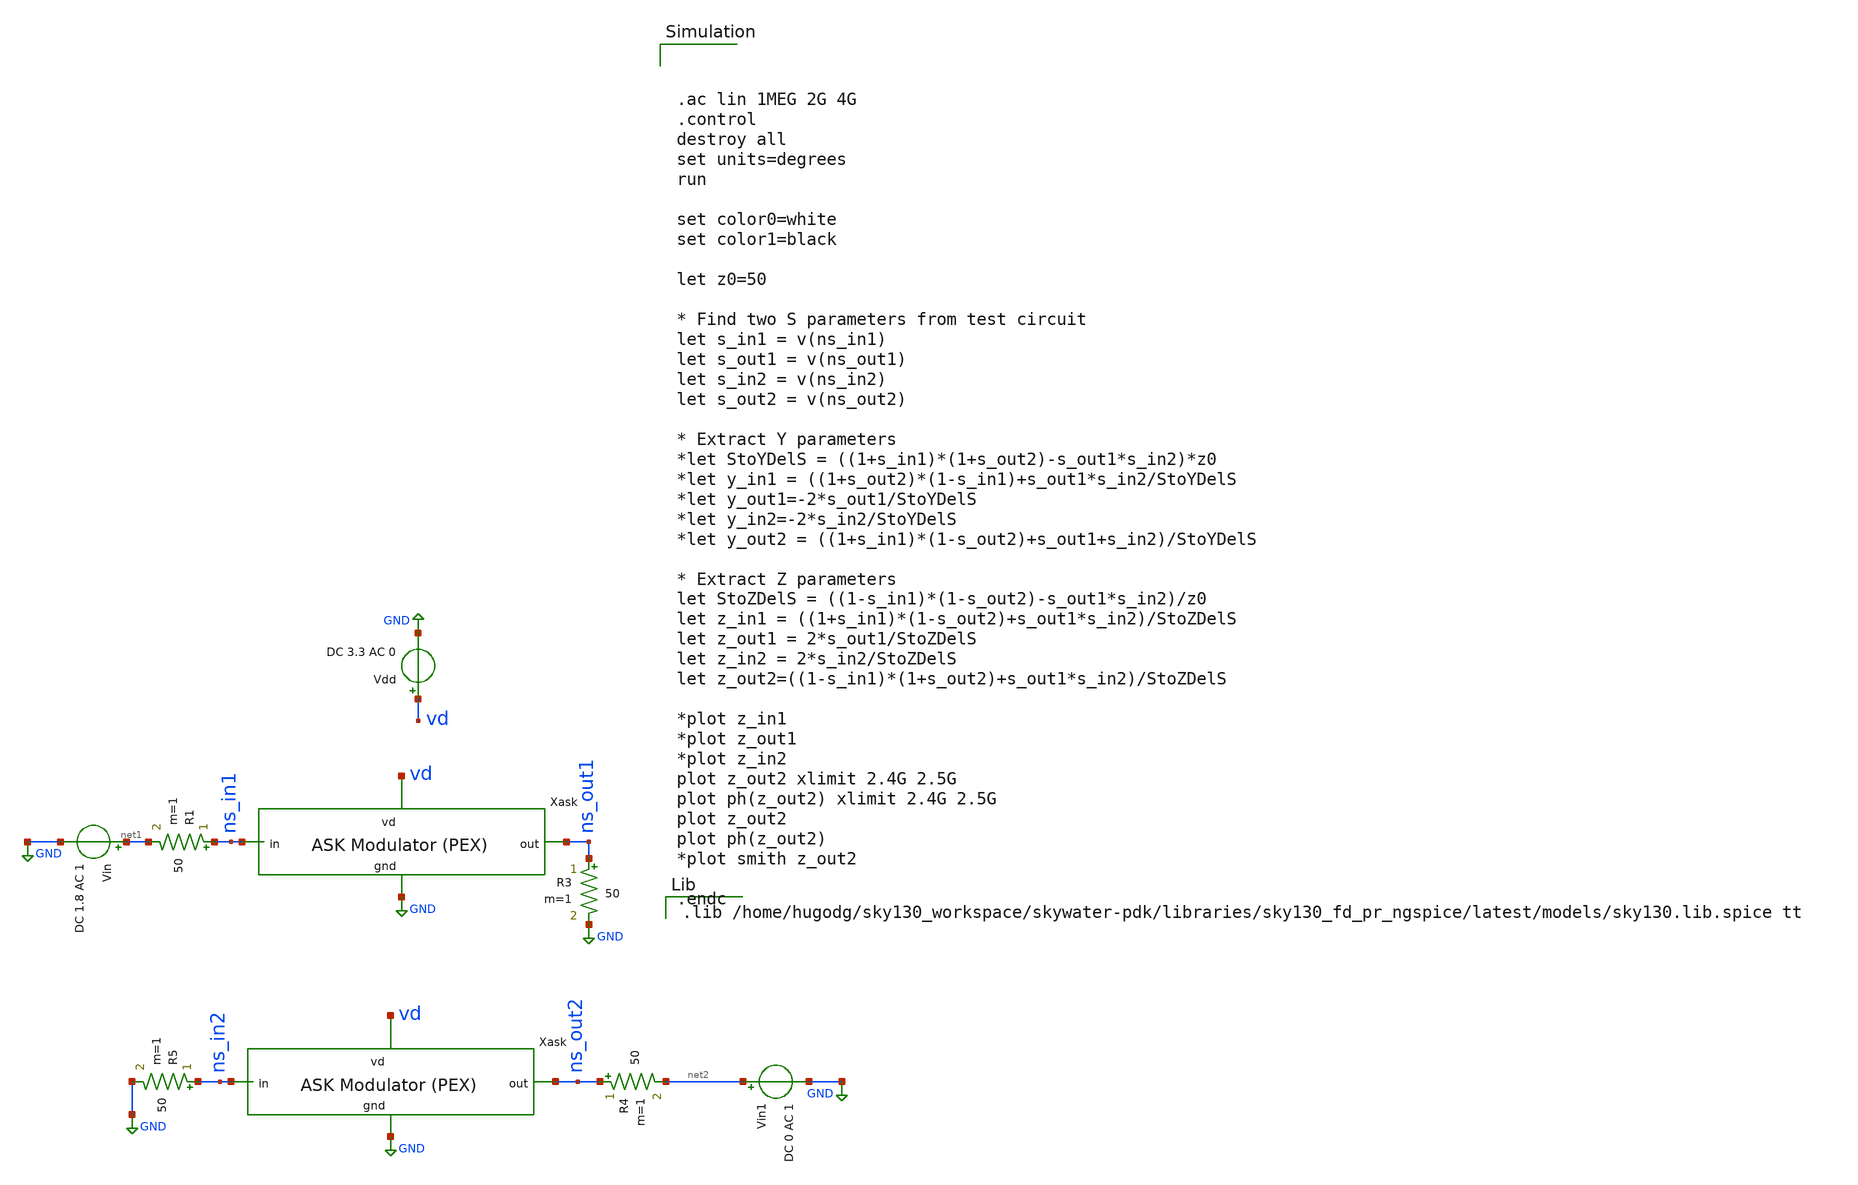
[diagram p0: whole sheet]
** sch_path: ask_modulator/xschem/ask-modulator-pex_tb-ac.sch
**.subckt ask-modulator-pex_tb-ac
Vdd vd GND DC 3.3 AC 0
Vin net1 GND DC 1.8 AC 1
Vin1 net2 GND DC 0 AC 1
R1 ns_in1 net1 50 m=1
R3 ns_out1 GND 50 m=1
R4 ns_out2 net2 50 m=1
R5 ns_in2 GND 50 m=1
x1 vd ns_out1 ns_in1 GND ask-modulator-pex
x2 vd ns_out2 ns_in2 GND ask-modulator-pex
**** begin user architecture code



.ac lin 1MEG 2G 4G
.control
destroy all
set units=degrees
run

set color0=white
set color1=black

let z0=50

* Find two S parameters from test circuit
let s_in1 = v(ns_in1)
let s_out1 = v(ns_out1)
let s_in2 = v(ns_in2)
let s_out2 = v(ns_out2)

* Extract Y parameters
*let StoYDelS = ((1+s_in1)*(1+s_out2)-s_out1*s_in2)*z0
*let y_in1 = ((1+s_out2)*(1-s_in1)+s_out1*s_in2/StoYDelS
*let y_out1=-2*s_out1/StoYDelS
*let y_in2=-2*s_in2/StoYDelS
*let y_out2 = ((1+s_in1)*(1-s_out2)+s_out1+s_in2)/StoYDelS

* Extract Z parameters
let StoZDelS = ((1-s_in1)*(1-s_out2)-s_out1*s_in2)/z0
let z_in1 = ((1+s_in1)*(1-s_out2)+s_out1*s_in2)/StoZDelS
let z_out1 = 2*s_out1/StoZDelS
let z_in2 = 2*s_in2/StoZDelS
let z_out2=((1-s_in1)*(1+s_out2)+s_out1*s_in2)/StoZDelS

*plot z_in1
*plot z_out1
*plot z_in2
plot z_out2 xlimit 2.4G 2.5G
plot ph(z_out2) xlimit 2.4G 2.5G
plot z_out2
plot ph(z_out2)
*plot smith z_out2

.endc


.lib /home/hugodg/sky130_workspace/skywater-pdk/libraries/sky130_fd_pr_ngspice/latest/models/sky130.lib.spice tt

**** end user architecture code
**.ends
.GLOBAL GND
.end
